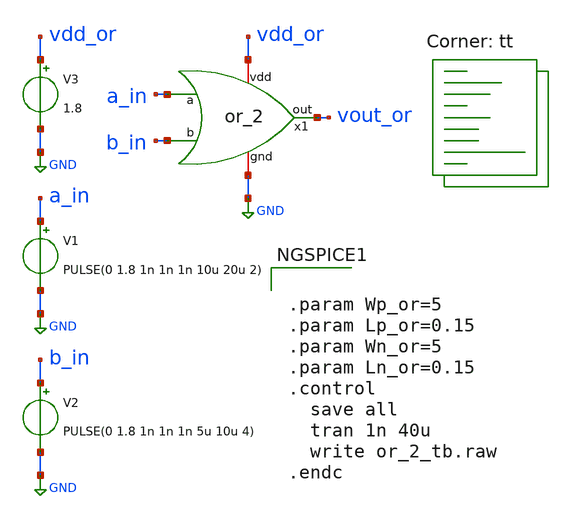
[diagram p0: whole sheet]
** sch_path: inhibitory/or_2_tb.sch
**.subckt or_2_tb
V1 a_in GND PULSE(0 1.8 1n 1n 1n 10u 20u 2)
V3 vdd_or GND 1.8
V2 b_in GND PULSE(0 1.8 1n 1n 1n 5u 10u 4)
x1 vdd_or a_in b_in vout_or GND or_2
**** begin user architecture code
.lib $::SKYWATER_MODELS/sky130.lib.spice tt


.param Wp_or=5
.param Lp_or=0.15
.param Wn_or=5
.param Ln_or=0.15
.control
  save all
  tran 1n 40u
  write or_2_tb.raw
.endc

**** end user architecture code
**.ends

* expanding   symbol:  /home/ricardo/RATT_repos/Proyectos_xschem/inhibitory/or_2.sym # of pins=5
** sym_path: inhibitory/or_2.sym
** sch_path: inhibitory/or_2.sch
.subckt or_2 vdd a b out gnd
*.iopin gnd
*.ipin a
*.ipin b
*.opin out
*.iopin vdd
XM1 net1 a vdd vdd sky130_fd_pr__pfet_01v8 L={Lp_or} W={Wp_or} nf=1 ad='int((nf+1)/2) * W/nf * 0.29'
+ as='int((nf+2)/2) * W/nf * 0.29' pd='2*int((nf+1)/2) * (W/nf + 0.29)' ps='2*int((nf+2)/2) * (W/nf + 0.29)'
+ nrd='0.29 / W' nrs='0.29 / W' sa=0 sb=0 sd=0 mult=1 m=1
XM2 net2 b gnd gnd sky130_fd_pr__nfet_01v8 L={Ln_or} W={Wn_or} nf=1 ad='int((nf+1)/2) * W/nf * 0.29'
+ as='int((nf+2)/2) * W/nf * 0.29' pd='2*int((nf+1)/2) * (W/nf + 0.29)' ps='2*int((nf+2)/2) * (W/nf + 0.29)'
+ nrd='0.29 / W' nrs='0.29 / W' sa=0 sb=0 sd=0 mult=1 m=1
XM3 net2 b net1 vdd sky130_fd_pr__pfet_01v8 L={Lp_or} W={Wp_or} nf=1 ad='int((nf+1)/2) * W/nf * 0.29'
+ as='int((nf+2)/2) * W/nf * 0.29' pd='2*int((nf+1)/2) * (W/nf + 0.29)' ps='2*int((nf+2)/2) * (W/nf + 0.29)'
+ nrd='0.29 / W' nrs='0.29 / W' sa=0 sb=0 sd=0 mult=1 m=1
XM4 net2 a gnd gnd sky130_fd_pr__nfet_01v8 L={Ln_or} W={Wn_or} nf=1 ad='int((nf+1)/2) * W/nf * 0.29'
+ as='int((nf+2)/2) * W/nf * 0.29' pd='2*int((nf+1)/2) * (W/nf + 0.29)' ps='2*int((nf+2)/2) * (W/nf + 0.29)'
+ nrd='0.29 / W' nrs='0.29 / W' sa=0 sb=0 sd=0 mult=1 m=1
XM5 out net2 gnd gnd sky130_fd_pr__nfet_01v8 L={Ln_or} W={Wn_or} nf=1 ad='int((nf+1)/2) * W/nf * 0.29'
+ as='int((nf+2)/2) * W/nf * 0.29' pd='2*int((nf+1)/2) * (W/nf + 0.29)' ps='2*int((nf+2)/2) * (W/nf + 0.29)'
+ nrd='0.29 / W' nrs='0.29 / W' sa=0 sb=0 sd=0 mult=1 m=1
XM6 out net2 vdd vdd sky130_fd_pr__pfet_01v8 L={Lp_or} W={Wp_or} nf=1 ad='int((nf+1)/2) * W/nf * 0.29'
+ as='int((nf+2)/2) * W/nf * 0.29' pd='2*int((nf+1)/2) * (W/nf + 0.29)' ps='2*int((nf+2)/2) * (W/nf + 0.29)'
+ nrd='0.29 / W' nrs='0.29 / W' sa=0 sb=0 sd=0 mult=1 m=1
.ends

.GLOBAL GND
.end
